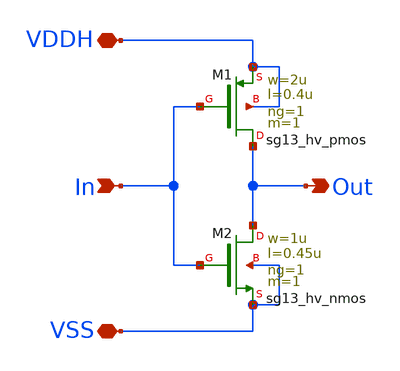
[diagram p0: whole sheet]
** sch_path: sar_adc/xschem/blocks/logic_elements/inverter_hv/inverter_hv.sch
**.subckt inverter_hv In VDDH VSS Out
*.ipin In
*.iopin VDDH
*.iopin VSS
*.opin Out
XM1 Out In VDDH VDDH sg13_hv_pmos w=2u l=0.4u ng=1 m=1 mm_ok=1
XM2 Out In VSS VSS sg13_hv_nmos w=1u l=0.45u ng=1 m=1 mm_ok=1
**.ends
.end
